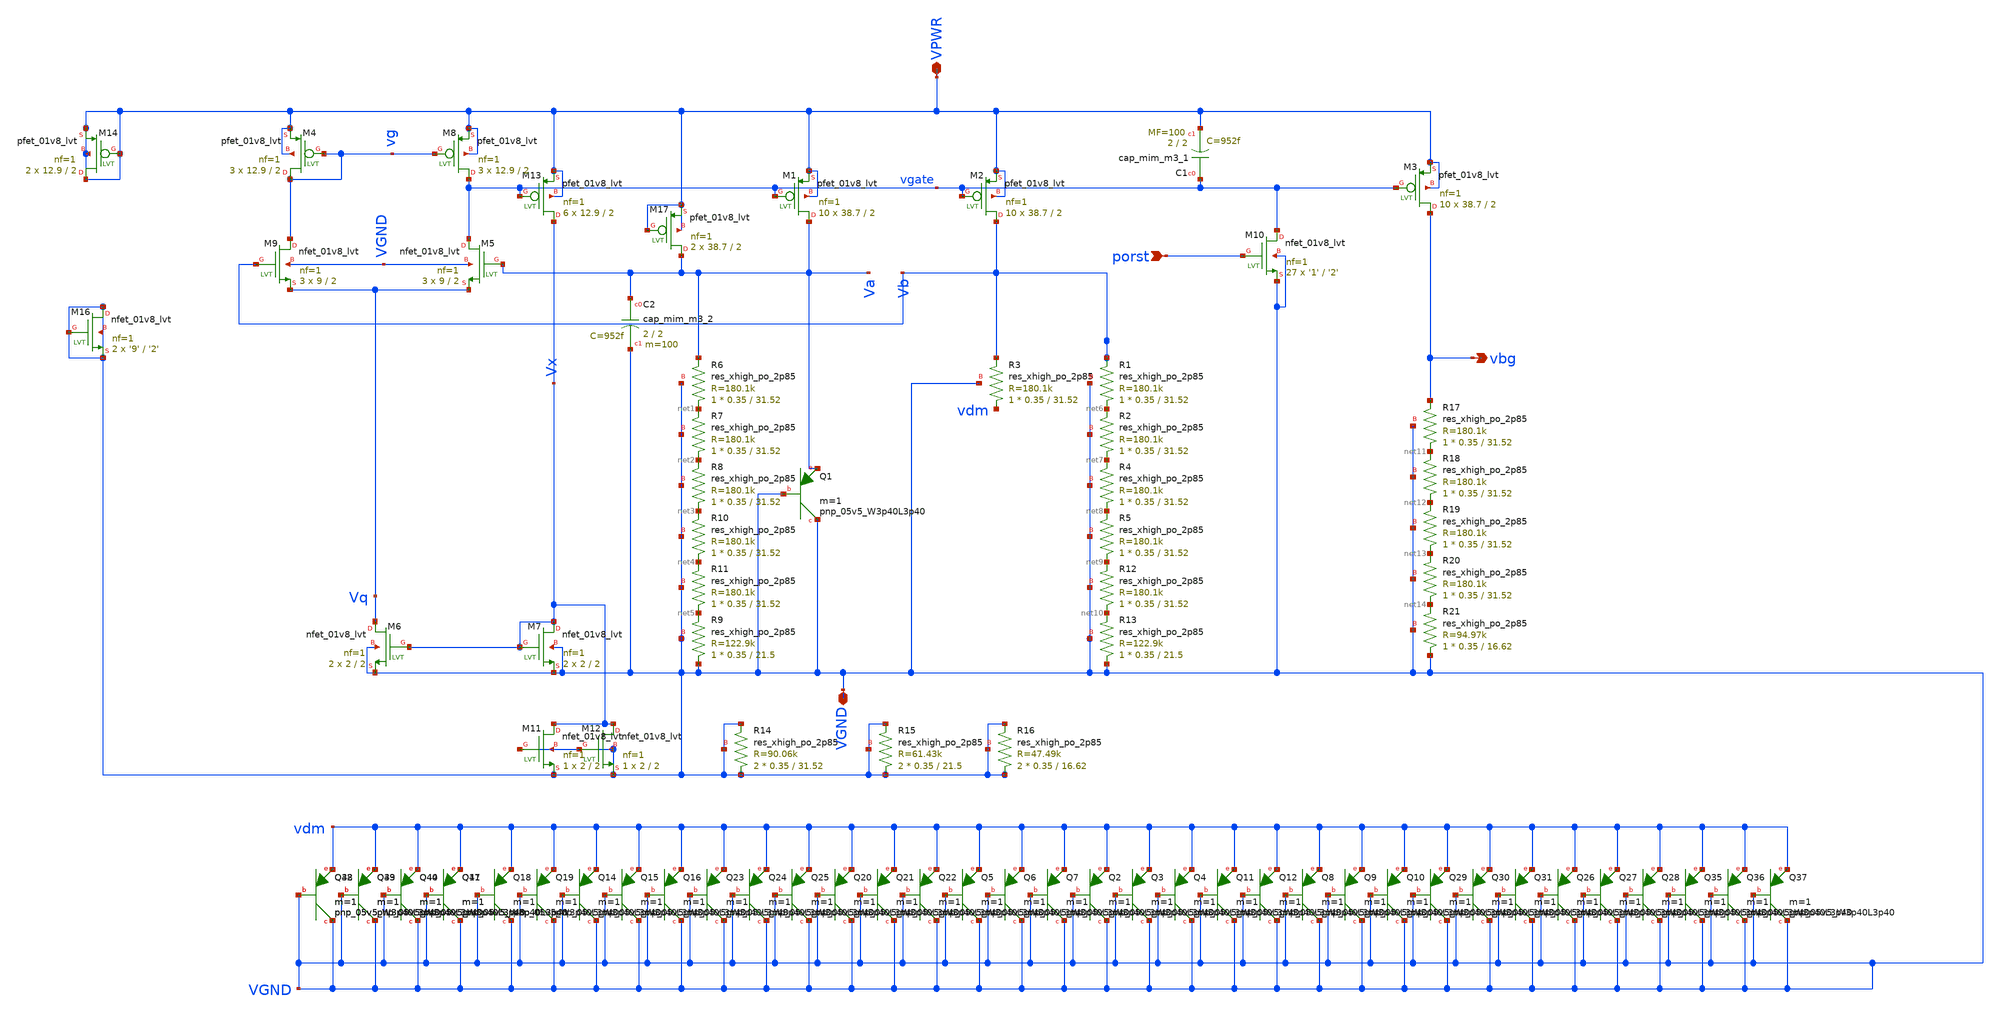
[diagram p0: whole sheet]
** sch_path: xschem/xschem/bandgaptop_flat_io.sch
**.subckt bandgaptop_flat_io porst vbg VGND VPWR
*.ipin porst
*.opin vbg
*.iopin VGND
*.iopin VPWR
XM5 vgate Va Vq VGND sky130_fd_pr__nfet_01v8_lvt L=2 W=9 nf=1 ad='int((nf+1)/2) * W/nf * 0.29' as='int((nf+2)/2) * W/nf * 0.29'
+ pd='2*int((nf+1)/2) * (W/nf + 0.29)' ps='2*int((nf+2)/2) * (W/nf + 0.29)' nrd='0.29 / W' nrs='0.29 / W'
+ sa=0 sb=0 sd=0 mult=3 m=3
XM6 Vq Vx VGND VGND sky130_fd_pr__nfet_01v8_lvt L=2 W=2 nf=1 ad='int((nf+1)/2) * W/nf * 0.29' as='int((nf+2)/2) * W/nf * 0.29'
+ pd='2*int((nf+1)/2) * (W/nf + 0.29)' ps='2*int((nf+2)/2) * (W/nf + 0.29)' nrd='0.29 / W' nrs='0.29 / W'
+ sa=0 sb=0 sd=0 mult=2 m=2
XM9 vg Vb Vq VGND sky130_fd_pr__nfet_01v8_lvt L=2 W=9 nf=1 ad='int((nf+1)/2) * W/nf * 0.29' as='int((nf+2)/2) * W/nf * 0.29'
+ pd='2*int((nf+1)/2) * (W/nf + 0.29)' ps='2*int((nf+2)/2) * (W/nf + 0.29)' nrd='0.29 / W' nrs='0.29 / W'
+ sa=0 sb=0 sd=0 mult=3 m=3
XM7 Vx Vx VGND VGND sky130_fd_pr__nfet_01v8_lvt L=2 W=2 nf=1 ad='int((nf+1)/2) * W/nf * 0.29' as='int((nf+2)/2) * W/nf * 0.29'
+ pd='2*int((nf+1)/2) * (W/nf + 0.29)' ps='2*int((nf+2)/2) * (W/nf + 0.29)' nrd='0.29 / W' nrs='0.29 / W'
+ sa=0 sb=0 sd=0 mult=2 m=2
XM13 Vx vgate VPWR VPWR sky130_fd_pr__pfet_01v8_lvt L=2 W=12.9 nf=1 ad='int((nf+1)/2) * W/nf * 0.29'
+ as='int((nf+2)/2) * W/nf * 0.29' pd='2*int((nf+1)/2) * (W/nf + 0.29)' ps='2*int((nf+2)/2) * (W/nf + 0.29)'
+ nrd='0.29 / W' nrs='0.29 / W' sa=0 sb=0 sd=0 mult=6 m=6
XM1 Va vgate VPWR VPWR sky130_fd_pr__pfet_01v8_lvt L=2 W=38.7 nf=1 ad='int((nf+1)/2) * W/nf * 0.29' as='int((nf+2)/2) * W/nf * 0.29'
+ pd='2*int((nf+1)/2) * (W/nf + 0.29)' ps='2*int((nf+2)/2) * (W/nf + 0.29)' nrd='0.29 / W' nrs='0.29 / W'
+ sa=0 sb=0 sd=0 mult=10 m=10
XM2 Vb vgate VPWR VPWR sky130_fd_pr__pfet_01v8_lvt L=2 W=38.7 nf=1 ad='int((nf+1)/2) * W/nf * 0.29' as='int((nf+2)/2) * W/nf * 0.29'
+ pd='2*int((nf+1)/2) * (W/nf + 0.29)' ps='2*int((nf+2)/2) * (W/nf + 0.29)' nrd='0.29 / W' nrs='0.29 / W'
+ sa=0 sb=0 sd=0 mult=10 m=10
XM3 vbg vgate VPWR VPWR sky130_fd_pr__pfet_01v8_lvt L=2 W=38.7 nf=1 ad='int((nf+1)/2) * W/nf * 0.29'
+ as='int((nf+2)/2) * W/nf * 0.29' pd='2*int((nf+1)/2) * (W/nf + 0.29)' ps='2*int((nf+2)/2) * (W/nf + 0.29)'
+ nrd='0.29 / W' nrs='0.29 / W' sa=0 sb=0 sd=0 mult=10 m=10
XM4 vg vg VPWR VPWR sky130_fd_pr__pfet_01v8_lvt L=2 W=12.9 nf=1 ad='int((nf+1)/2) * W/nf * 0.29' as='int((nf+2)/2) * W/nf * 0.29'
+ pd='2*int((nf+1)/2) * (W/nf + 0.29)' ps='2*int((nf+2)/2) * (W/nf + 0.29)' nrd='0.29 / W' nrs='0.29 / W'
+ sa=0 sb=0 sd=0 mult=3 m=3
XM8 vgate vg VPWR VPWR sky130_fd_pr__pfet_01v8_lvt L=2 W=12.9 nf=1 ad='int((nf+1)/2) * W/nf * 0.29' as='int((nf+2)/2) * W/nf * 0.29'
+ pd='2*int((nf+1)/2) * (W/nf + 0.29)' ps='2*int((nf+2)/2) * (W/nf + 0.29)' nrd='0.29 / W' nrs='0.29 / W'
+ sa=0 sb=0 sd=0 mult=3 m=3
XM10 vgate porst VGND VGND sky130_fd_pr__nfet_01v8_lvt L='2' W='1' nf=1 ad='int((nf+1)/2) * W/nf * 0.29'
+ as='int((nf+2)/2) * W/nf * 0.29' pd='2*int((nf+1)/2) * (W/nf + 0.29)' ps='2*int((nf+2)/2) * (W/nf + 0.29)'
+ nrd='0.29 / W' nrs='0.29 / W' sa=0 sb=0 sd=0 mult=27 m=27
XR6 net1 Va VGND sky130_fd_pr__res_xhigh_po_2p85 L=31.52 mult=1 m=1
XR7 net2 net1 VGND sky130_fd_pr__res_xhigh_po_2p85 L=31.52 mult=1 m=1
XR8 net3 net2 VGND sky130_fd_pr__res_xhigh_po_2p85 L=31.52 mult=1 m=1
XR10 net4 net3 VGND sky130_fd_pr__res_xhigh_po_2p85 L=31.52 mult=1 m=1
XR11 net5 net4 VGND sky130_fd_pr__res_xhigh_po_2p85 L=31.52 mult=1 m=1
XR9 VGND net5 VGND sky130_fd_pr__res_xhigh_po_2p85 L=21.5 mult=1 m=1
XR3 vdm Vb VGND sky130_fd_pr__res_xhigh_po_2p85 L=31.52 mult=1 m=1
XR1 net6 Vb VGND sky130_fd_pr__res_xhigh_po_2p85 L=31.52 mult=1 m=1
XR2 net7 net6 VGND sky130_fd_pr__res_xhigh_po_2p85 L=31.52 mult=1 m=1
XR4 net8 net7 VGND sky130_fd_pr__res_xhigh_po_2p85 L=31.52 mult=1 m=1
XR5 net9 net8 VGND sky130_fd_pr__res_xhigh_po_2p85 L=31.52 mult=1 m=1
XR12 net10 net9 VGND sky130_fd_pr__res_xhigh_po_2p85 L=31.52 mult=1 m=1
XR13 VGND net10 VGND sky130_fd_pr__res_xhigh_po_2p85 L=21.5 mult=1 m=1
XR17 net11 vbg VGND sky130_fd_pr__res_xhigh_po_2p85 L=31.52 mult=1 m=1
XR18 net12 net11 VGND sky130_fd_pr__res_xhigh_po_2p85 L=31.52 mult=1 m=1
XR19 net13 net12 VGND sky130_fd_pr__res_xhigh_po_2p85 L=31.52 mult=1 m=1
XR20 net14 net13 VGND sky130_fd_pr__res_xhigh_po_2p85 L=31.52 mult=1 m=1
XR21 VGND net14 VGND sky130_fd_pr__res_xhigh_po_2p85 L=16.62 mult=1 m=1
XR14 VGND VGND VGND sky130_fd_pr__res_xhigh_po_2p85 L=31.52 mult=2 m=2
XR15 VGND VGND VGND sky130_fd_pr__res_xhigh_po_2p85 L=21.5 mult=2 m=2
XR16 VGND VGND VGND sky130_fd_pr__res_xhigh_po_2p85 L=16.62 mult=2 m=2
XM11 Vx VGND VGND VGND sky130_fd_pr__nfet_01v8_lvt L=2 W=2 nf=1 ad='int((nf+1)/2) * W/nf * 0.29' as='int((nf+2)/2) * W/nf * 0.29'
+ pd='2*int((nf+1)/2) * (W/nf + 0.29)' ps='2*int((nf+2)/2) * (W/nf + 0.29)' nrd='0.29 / W' nrs='0.29 / W'
+ sa=0 sb=0 sd=0 mult=1 m=1
XM12 Vx VGND VGND VGND sky130_fd_pr__nfet_01v8_lvt L=2 W=2 nf=1 ad='int((nf+1)/2) * W/nf * 0.29' as='int((nf+2)/2) * W/nf * 0.29'
+ pd='2*int((nf+1)/2) * (W/nf + 0.29)' ps='2*int((nf+2)/2) * (W/nf + 0.29)' nrd='0.29 / W' nrs='0.29 / W'
+ sa=0 sb=0 sd=0 mult=1 m=1
XM14 VPWR VPWR VPWR VPWR sky130_fd_pr__pfet_01v8_lvt L=2 W=12.9 nf=1 ad='int((nf+1)/2) * W/nf * 0.29'
+ as='int((nf+2)/2) * W/nf * 0.29' pd='2*int((nf+1)/2) * (W/nf + 0.29)' ps='2*int((nf+2)/2) * (W/nf + 0.29)'
+ nrd='0.29 / W' nrs='0.29 / W' sa=0 sb=0 sd=0 mult=2 m=2
XM16 VGND VGND VGND VGND sky130_fd_pr__nfet_01v8_lvt L='2' W='9' nf=1 ad='int((nf+1)/2) * W/nf * 0.29'
+ as='int((nf+2)/2) * W/nf * 0.29' pd='2*int((nf+1)/2) * (W/nf + 0.29)' ps='2*int((nf+2)/2) * (W/nf + 0.29)'
+ nrd='0.29 / W' nrs='0.29 / W' sa=0 sb=0 sd=0 mult=2 m=2
XM17 Va VPWR VPWR VPWR sky130_fd_pr__pfet_01v8_lvt L=2 W=38.7 nf=1 ad='int((nf+1)/2) * W/nf * 0.29' as='int((nf+2)/2) * W/nf * 0.29'
+ pd='2*int((nf+1)/2) * (W/nf + 0.29)' ps='2*int((nf+2)/2) * (W/nf + 0.29)' nrd='0.29 / W' nrs='0.29 / W'
+ sa=0 sb=0 sd=0 mult=2 m=2
XC1 vgate VPWR sky130_fd_pr__cap_mim_m3_1 W=2 L=2 MF=100 m=100
XC2 Va VGND sky130_fd_pr__cap_mim_m3_2 W=2 L=2 MF=100 m=100
XQ1 VGND VGND Va sky130_fd_pr__pnp_05v5_W3p40L3p40 m=1
XQ2 VGND VGND vdm sky130_fd_pr__pnp_05v5_W3p40L3p40 m=1
XQ3 VGND VGND vdm sky130_fd_pr__pnp_05v5_W3p40L3p40 m=1
XQ4 VGND VGND vdm sky130_fd_pr__pnp_05v5_W3p40L3p40 m=1
XQ5 VGND VGND vdm sky130_fd_pr__pnp_05v5_W3p40L3p40 m=1
XQ6 VGND VGND vdm sky130_fd_pr__pnp_05v5_W3p40L3p40 m=1
XQ7 VGND VGND vdm sky130_fd_pr__pnp_05v5_W3p40L3p40 m=1
XQ8 VGND VGND vdm sky130_fd_pr__pnp_05v5_W3p40L3p40 m=1
XQ9 VGND VGND vdm sky130_fd_pr__pnp_05v5_W3p40L3p40 m=1
XQ10 VGND VGND vdm sky130_fd_pr__pnp_05v5_W3p40L3p40 m=1
XQ11 VGND VGND vdm sky130_fd_pr__pnp_05v5_W3p40L3p40 m=1
XQ12 VGND VGND vdm sky130_fd_pr__pnp_05v5_W3p40L3p40 m=1
XQ14 VGND VGND vdm sky130_fd_pr__pnp_05v5_W3p40L3p40 m=1
XQ15 VGND VGND vdm sky130_fd_pr__pnp_05v5_W3p40L3p40 m=1
XQ16 VGND VGND vdm sky130_fd_pr__pnp_05v5_W3p40L3p40 m=1
XQ17 VGND VGND vdm sky130_fd_pr__pnp_05v5_W3p40L3p40 m=1
XQ18 VGND VGND vdm sky130_fd_pr__pnp_05v5_W3p40L3p40 m=1
XQ19 VGND VGND vdm sky130_fd_pr__pnp_05v5_W3p40L3p40 m=1
XQ20 VGND VGND vdm sky130_fd_pr__pnp_05v5_W3p40L3p40 m=1
XQ21 VGND VGND vdm sky130_fd_pr__pnp_05v5_W3p40L3p40 m=1
XQ22 VGND VGND vdm sky130_fd_pr__pnp_05v5_W3p40L3p40 m=1
XQ23 VGND VGND vdm sky130_fd_pr__pnp_05v5_W3p40L3p40 m=1
XQ24 VGND VGND vdm sky130_fd_pr__pnp_05v5_W3p40L3p40 m=1
XQ25 VGND VGND vdm sky130_fd_pr__pnp_05v5_W3p40L3p40 m=1
XQ26 VGND VGND vdm sky130_fd_pr__pnp_05v5_W3p40L3p40 m=1
XQ27 VGND VGND vdm sky130_fd_pr__pnp_05v5_W3p40L3p40 m=1
XQ28 VGND VGND vdm sky130_fd_pr__pnp_05v5_W3p40L3p40 m=1
XQ29 VGND VGND vdm sky130_fd_pr__pnp_05v5_W3p40L3p40 m=1
XQ30 VGND VGND vdm sky130_fd_pr__pnp_05v5_W3p40L3p40 m=1
XQ31 VGND VGND vdm sky130_fd_pr__pnp_05v5_W3p40L3p40 m=1
XQ35 VGND VGND vdm sky130_fd_pr__pnp_05v5_W3p40L3p40 m=1
XQ36 VGND VGND vdm sky130_fd_pr__pnp_05v5_W3p40L3p40 m=1
XQ37 VGND VGND vdm sky130_fd_pr__pnp_05v5_W3p40L3p40 m=1
XQ38 VGND VGND vdm sky130_fd_pr__pnp_05v5_W3p40L3p40 m=1
XQ39 VGND VGND vdm sky130_fd_pr__pnp_05v5_W3p40L3p40 m=1
XQ40 VGND VGND vdm sky130_fd_pr__pnp_05v5_W3p40L3p40 m=1
XQ41 VGND VGND vdm sky130_fd_pr__pnp_05v5_W3p40L3p40 m=1
XQ42 VGND VGND vdm sky130_fd_pr__pnp_05v5_W3p40L3p40 m=1
XQ43 VGND VGND vdm sky130_fd_pr__pnp_05v5_W3p40L3p40 m=1
XQ44 VGND VGND vdm sky130_fd_pr__pnp_05v5_W3p40L3p40 m=1
**.ends
.end
